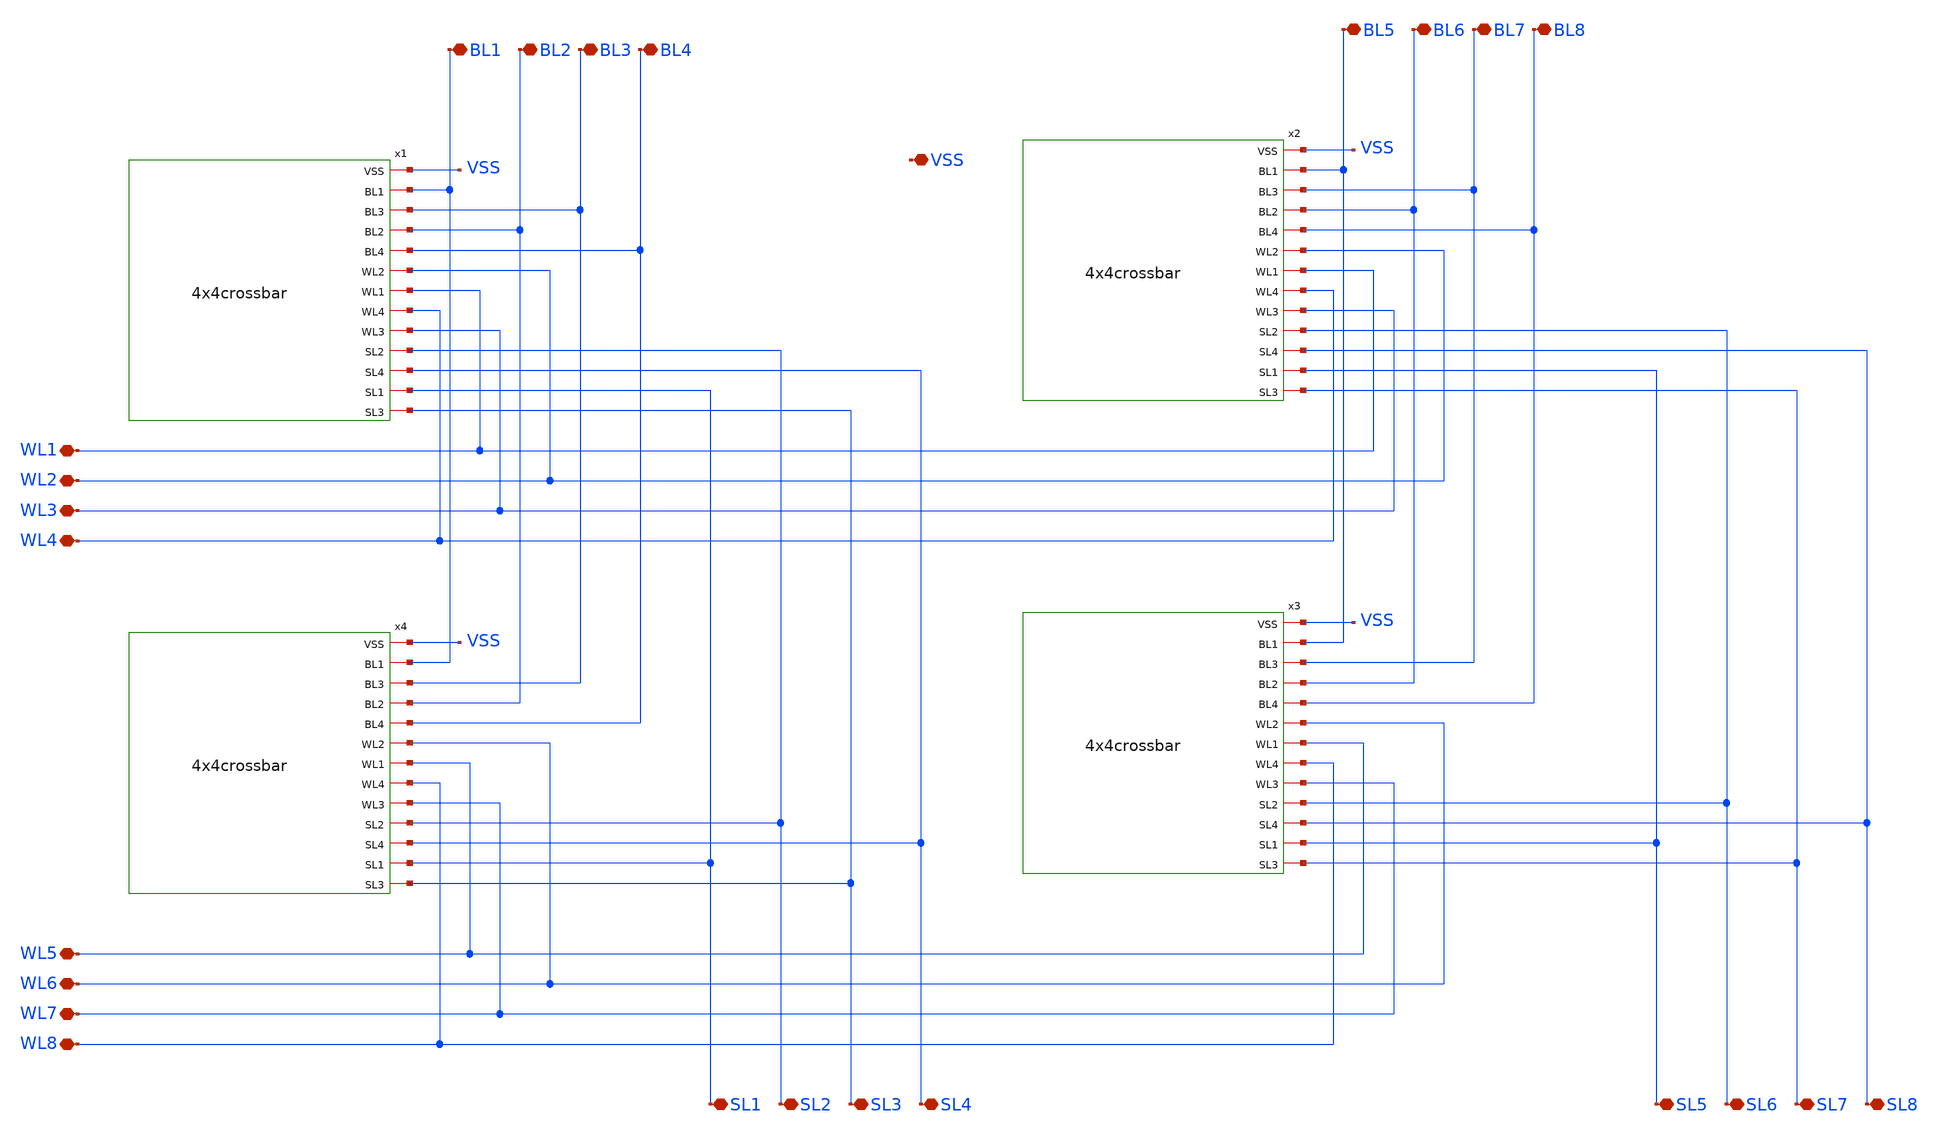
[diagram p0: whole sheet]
** sch_path: xschem/Crossbar/8x8crossbar.sch
**.subckt 8x8crossbar BL1 BL2 BL3 BL4 BL5 BL6 BL7 BL8 SL1 WL1 WL2 WL3 WL4 WL5 WL6 WL7 WL8 SL2 SL3
*+ SL4 SL5 SL6 SL7 SL8 VSS
*.iopin BL1
*.iopin BL2
*.iopin BL3
*.iopin BL4
*.iopin BL5
*.iopin BL6
*.iopin BL7
*.iopin BL8
*.iopin SL1
*.iopin WL1
*.iopin WL2
*.iopin WL3
*.iopin WL4
*.iopin WL5
*.iopin WL6
*.iopin WL7
*.iopin WL8
*.iopin SL2
*.iopin SL3
*.iopin SL4
*.iopin SL5
*.iopin SL6
*.iopin SL7
*.iopin SL8
*.iopin VSS
x1 VSS BL1 BL3 BL2 BL4 WL2 WL1 WL4 WL3 SL2 SL4 SL1 SL3 4x4crossbar
x2 VSS BL5 BL7 BL6 BL8 WL2 WL1 WL4 WL3 SL6 SL8 SL5 SL7 4x4crossbar
x3 VSS BL5 BL7 BL6 BL8 WL6 WL5 WL8 WL7 SL6 SL8 SL5 SL7 4x4crossbar
x4 VSS BL1 BL3 BL2 BL4 WL6 WL5 WL8 WL7 SL2 SL4 SL1 SL3 4x4crossbar
**.ends
.end
